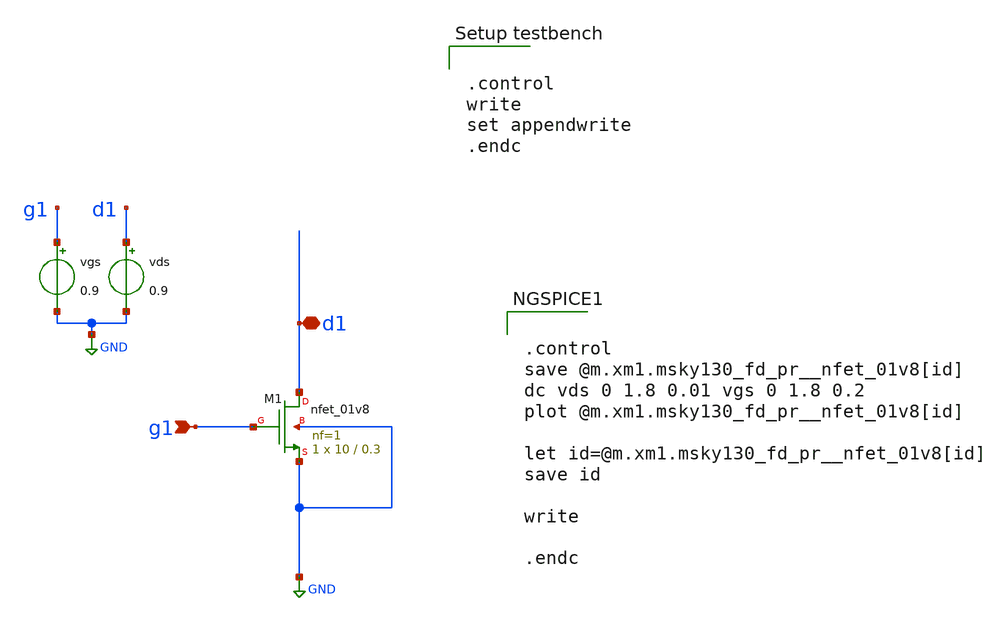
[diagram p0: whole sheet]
** sch_path: samples/sky130/nmos/test/nmos_charac.sch

*.lib $env(PDK_ROOT)/$env(PDK)/libs.tech/ngspice/sky130.lib.spice tt
.lib $env(PDK_ROOT)/$env(PDK)/libs.tech/ngspice/sky130.lib.spice.tt.red tt


.control
write
set appendwrite
.endc


**.subckt nmos_charac g1 d1
*.ipin g1
*.iopin d1
XM1 d1 g1 GND GND sky130_fd_pr__nfet_01v8 L=0.3 W=10 nf=1 ad='int((nf+1)/2) * W/nf * 0.29' as='int((nf+2)/2) * W/nf * 0.29'
+ pd='2*int((nf+1)/2) * (W/nf + 0.29)' ps='2*int((nf+2)/2) * (W/nf + 0.29)' nrd='0.29 / W' nrs='0.29 / W'
+ sa=0 sb=0 sd=0 mult=1 m=1
vgs g1 GND 0.9
vds d1 GND 0.9
**** begin user architecture code


.control
save @m.xm1.msky130_fd_pr__nfet_01v8[id]
dc vds 0 1.8 0.01 vgs 0 1.8 0.2
plot @m.xm1.msky130_fd_pr__nfet_01v8[id]

let id=@m.xm1.msky130_fd_pr__nfet_01v8[id]
save id

write

.endc


**** end user architecture code
**.ends
.GLOBAL GND
.end
